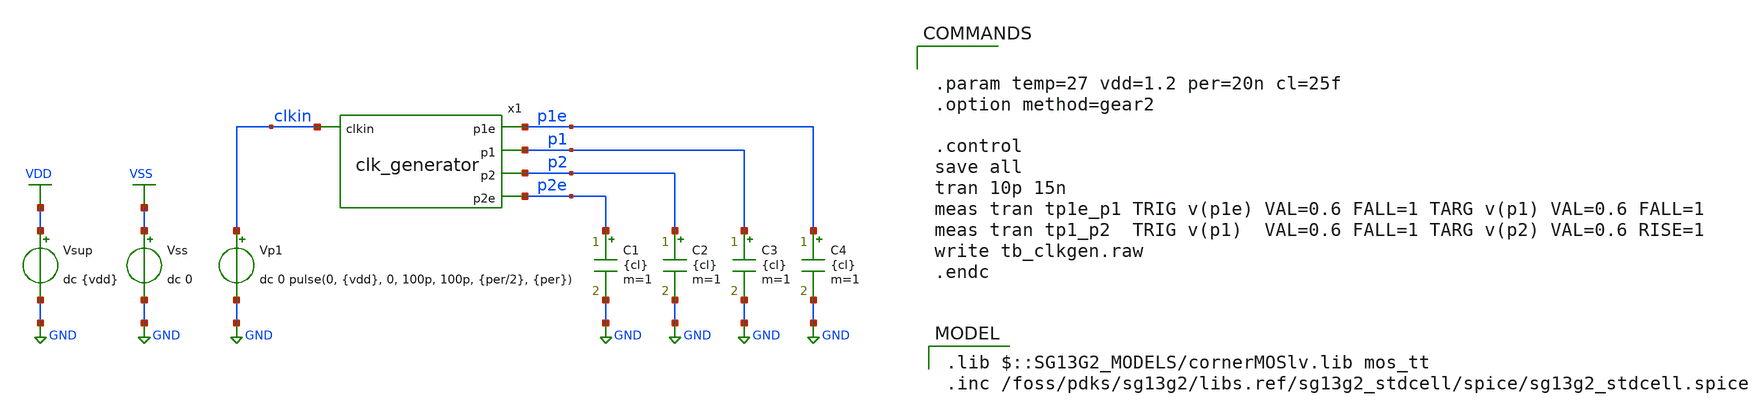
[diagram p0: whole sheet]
** sch_path: schematics/tb_clkgen.sch
**.subckt tb_clkgen
Vsup VDD GND dc {vdd}
Vss VSS GND dc 0
Vp1 clkin GND dc 0 pulse(0, {vdd}, 0, 100p, 100p, {per/2}, {per})
C1 p2e GND {cl} m=1
C2 p2 GND {cl} m=1
C3 p1 GND {cl} m=1
C4 p1e GND {cl} m=1
x1 p1e clkin p1 p2 p2e clk_generator
**** begin user architecture code


.param temp=27 vdd=1.2 per=20n cl=25f
.option method=gear2

.control
save all
tran 10p 15n
meas tran tp1e_p1 TRIG v(p1e) VAL=0.6 FALL=1 TARG v(p1) VAL=0.6 FALL=1
meas tran tp1_p2  TRIG v(p1)  VAL=0.6 FALL=1 TARG v(p2) VAL=0.6 RISE=1
write tb_clkgen.raw
.endc


 .lib $::SG13G2_MODELS/cornerMOSlv.lib mos_tt
.inc /foss/pdks/sg13g2/libs.ref/sg13g2_stdcell/spice/sg13g2_stdcell.spice

**** end user architecture code
**.ends
.GLOBAL VDD
.GLOBAL GND
.GLOBAL VSS
.end
